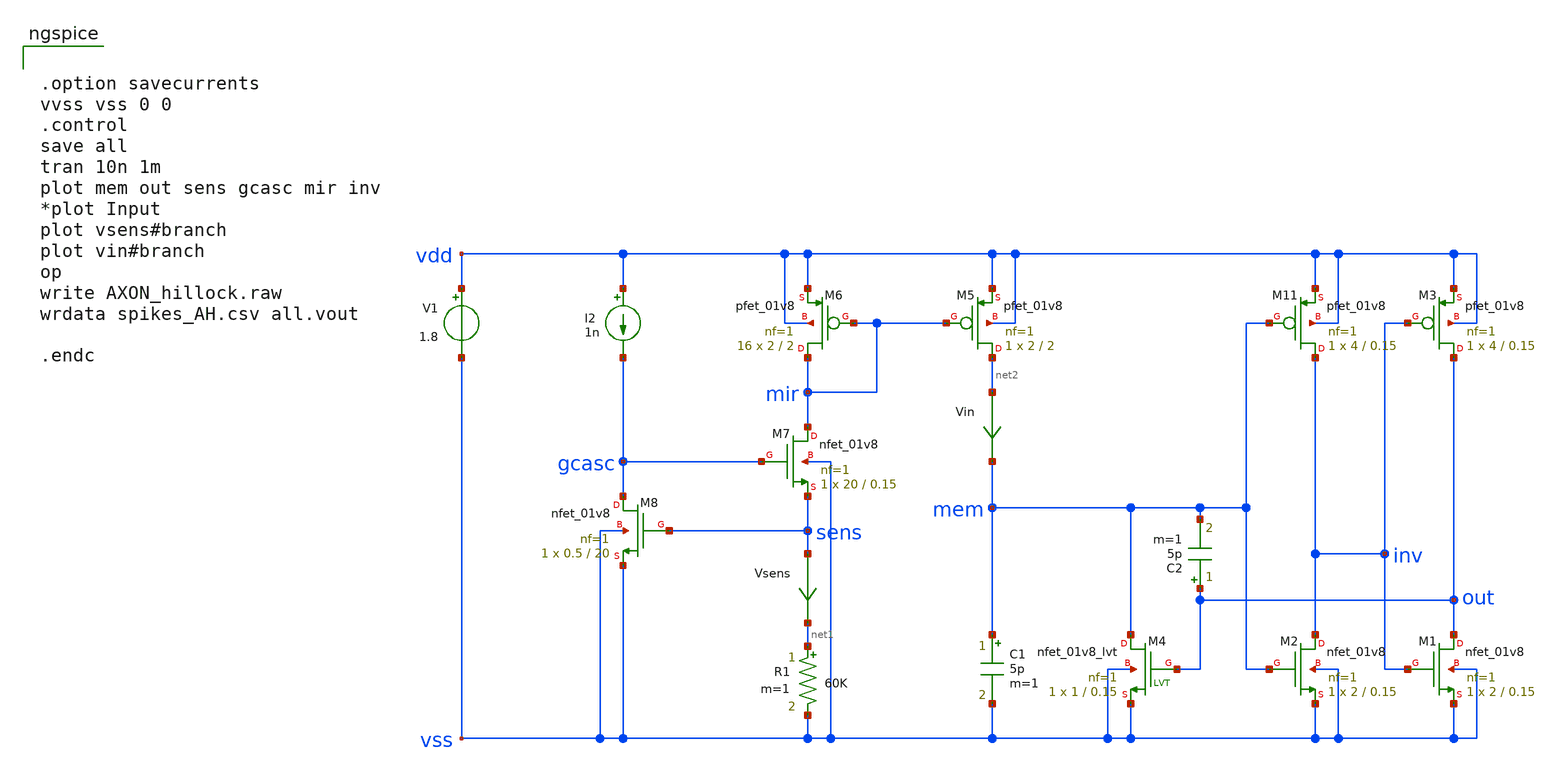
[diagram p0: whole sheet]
** sch_path: circuits/Axon_Hillock.sch
* Copyright 2020 Stefan Frederik Schippers
* Licensed under the Apache License, Version 2.0 (the "License");
* you may not use this file except in compliance with the License.
* You may obtain a copy of the License at
* https://www.apache.org/licenses/LICENSE-2.0
* Unless required by applicable law or agreed to in writing, software
* distributed under the License is distributed on an "AS IS" BASIS,
* WITHOUT WARRANTIES OR CONDITIONS OF ANY KIND, either express or implied.
* See the License for the specific language governing permissions and
* limitations under the License.
**.subckt Axon_Hillock
XM2 inv mem vss vss sky130_fd_pr__nfet_01v8 L=0.15 W=2 nf=1 ad='int((1 + 1)/2) * 2 / 1 * 0.29' as='int((1 + 2)/2) * 2 / 1 * 0.29'
+ pd='2*int((1 + 1)/2) * (2 / 1 + 0.29)' ps='2*int((1 + 2)/2) * (2 / 1 + 0.29)' nrd='0.29 / 2 ' nrs='0.29 / 2 '
+ sa=0 sb=0 sd=0 mult=1 m=1
XM11 inv mem vdd vdd sky130_fd_pr__pfet_01v8 L=0.15 W=4 nf=1 ad='int((nf+1)/2) * W/nf * 0.29' as='int((nf+2)/2) * W/nf * 0.29'
+ pd='2*int((nf+1)/2) * (W/nf + 0.29)' ps='2*int((nf+2)/2) * (W/nf + 0.29)' nrd='0.29 / W' nrs='0.29 / W'
+ sa=0 sb=0 sd=0 mult=1 m=1
XM1 out inv vss vss sky130_fd_pr__nfet_01v8 L=0.15 W=2 nf=1 ad='int((1 + 1)/2) * 2 / 1 * 0.29' as='int((1 + 2)/2) * 2 / 1 * 0.29'
+ pd='2*int((1 + 1)/2) * (2 / 1 + 0.29)' ps='2*int((1 + 2)/2) * (2 / 1 + 0.29)' nrd='0.29 / 2 ' nrs='0.29 / 2 '
+ sa=0 sb=0 sd=0 mult=1 m=1
XM3 out inv vdd vdd sky130_fd_pr__pfet_01v8 L=0.15 W=4 nf=1 ad='int((nf+1)/2) * W/nf * 0.29' as='int((nf+2)/2) * W/nf * 0.29'
+ pd='2*int((nf+1)/2) * (W/nf + 0.29)' ps='2*int((nf+2)/2) * (W/nf + 0.29)' nrd='0.29 / W' nrs='0.29 / W'
+ sa=0 sb=0 sd=0 mult=1 m=1
C2 out mem 5p m=1
V1 vdd vss 1.8
I2 vdd gcasc 1n
C1 mem vss 5p m=1
Vsens sens net1 0
.save i(vsens)
R1 net1 vss 60K m=1
XM5 net2 mir vdd vdd sky130_fd_pr__pfet_01v8 L=2 W=2 nf=1 ad='int((nf+1)/2) * W/nf * 0.29' as='int((nf+2)/2) * W/nf * 0.29'
+ pd='2*int((nf+1)/2) * (W/nf + 0.29)' ps='2*int((nf+2)/2) * (W/nf + 0.29)' nrd='0.29 / W' nrs='0.29 / W'
+ sa=0 sb=0 sd=0 mult=1 m=1
XM6 mir mir vdd vdd sky130_fd_pr__pfet_01v8 L=2 W=2 nf=1 ad='int((nf+1)/2) * W/nf * 0.29' as='int((nf+2)/2) * W/nf * 0.29'
+ pd='2*int((nf+1)/2) * (W/nf + 0.29)' ps='2*int((nf+2)/2) * (W/nf + 0.29)' nrd='0.29 / W' nrs='0.29 / W'
+ sa=0 sb=0 sd=0 mult=16 m=16
XM4 mem out vss vss sky130_fd_pr__nfet_01v8_lvt L=0.15 W=1 nf=1 ad='int((1 + 1)/2) * 1 / 1 * 0.29' as='int((1 + 2)/2) * 1 / 1 * 0.29'
+ pd='2*int((1 + 1)/2) * (1 / 1 + 0.29)' ps='2*int((1 + 2)/2) * (1 / 1 + 0.29)' nrd='0.29 / 1 ' nrs='0.29 / 1 '
+ sa=0 sb=0 sd=0 mult=1 m=1
XM7 mir gcasc sens vss sky130_fd_pr__nfet_01v8 L=0.15 W=20 nf=1 ad='int((1 + 1)/2) * 20 / 1 * 0.29' as='int((1 + 2)/2) * 20 / 1 * 0.29'
+ pd='2*int((1 + 1)/2) * (20 / 1 + 0.29)' ps='2*int((1 + 2)/2) * (20 / 1 + 0.29)' nrd='0.29 / 20 ' nrs='0.29 / 20 '
+ sa=0 sb=0 sd=0 mult=1 m=1
XM8 gcasc sens vss vss sky130_fd_pr__nfet_01v8 L=20 W=0.5 nf=1 ad='int((1 + 1)/2) * 0.5 / 1 * 0.29' as='int((1 + 2)/2) * 0.5 / 1 * 0.29'
+ pd='2*int((1 + 1)/2) * (0.5 / 1 + 0.29)' ps='2*int((1 + 2)/2) * (0.5 / 1 + 0.29)' nrd='0.29 / 0.5 ' nrs='0.29 / 0.5 '
+ sa=0 sb=0 sd=0 mult=1 m=1
Vin net2 mem 0
.save i(vin)
**** begin user architecture code


.option savecurrents
vvss vss 0 0
.control
save all
tran 10n 1m
plot mem out sens gcasc mir inv
*plot Input
plot vsens#branch
plot vin#branch
op
write AXON_hillock.raw
wrdata spikes_AH.csv all.vout

.endc


 .lib $::SKYWATER_MODELS/models/sky130.lib.spice tt

.param mc_mm_switch=0
.param mc_pr_switch=1


**** end user architecture code
**.ends
.end
